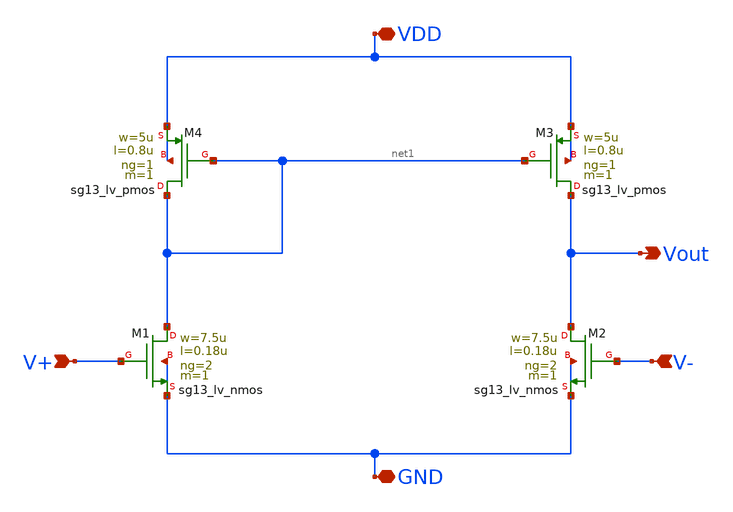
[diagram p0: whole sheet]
** sch_path: SSDOR_w_startup_1V_ihp/Ib_4u/Ib_4u_opamp/Ib_4u_opamp.sch
**.subckt Ib_4u_opamp VDD V+ V- GND Vout
*.iopin VDD
*.ipin V+
*.ipin V-
*.iopin GND
*.opin Vout
XM1 net1 V+ GND GND sg13_lv_nmos w=7.5u l=0.18u ng=2 m=1 mm_ok=1
XM2 Vout V- GND GND sg13_lv_nmos w=7.5u l=0.18u ng=2 m=1 mm_ok=1
XM3 Vout net1 VDD VDD sg13_lv_pmos w=5u l=0.8u ng=1 m=1 mm_ok=1
XM4 net1 net1 VDD VDD sg13_lv_pmos w=5u l=0.8u ng=1 m=1 mm_ok=1
**.ends
.end
